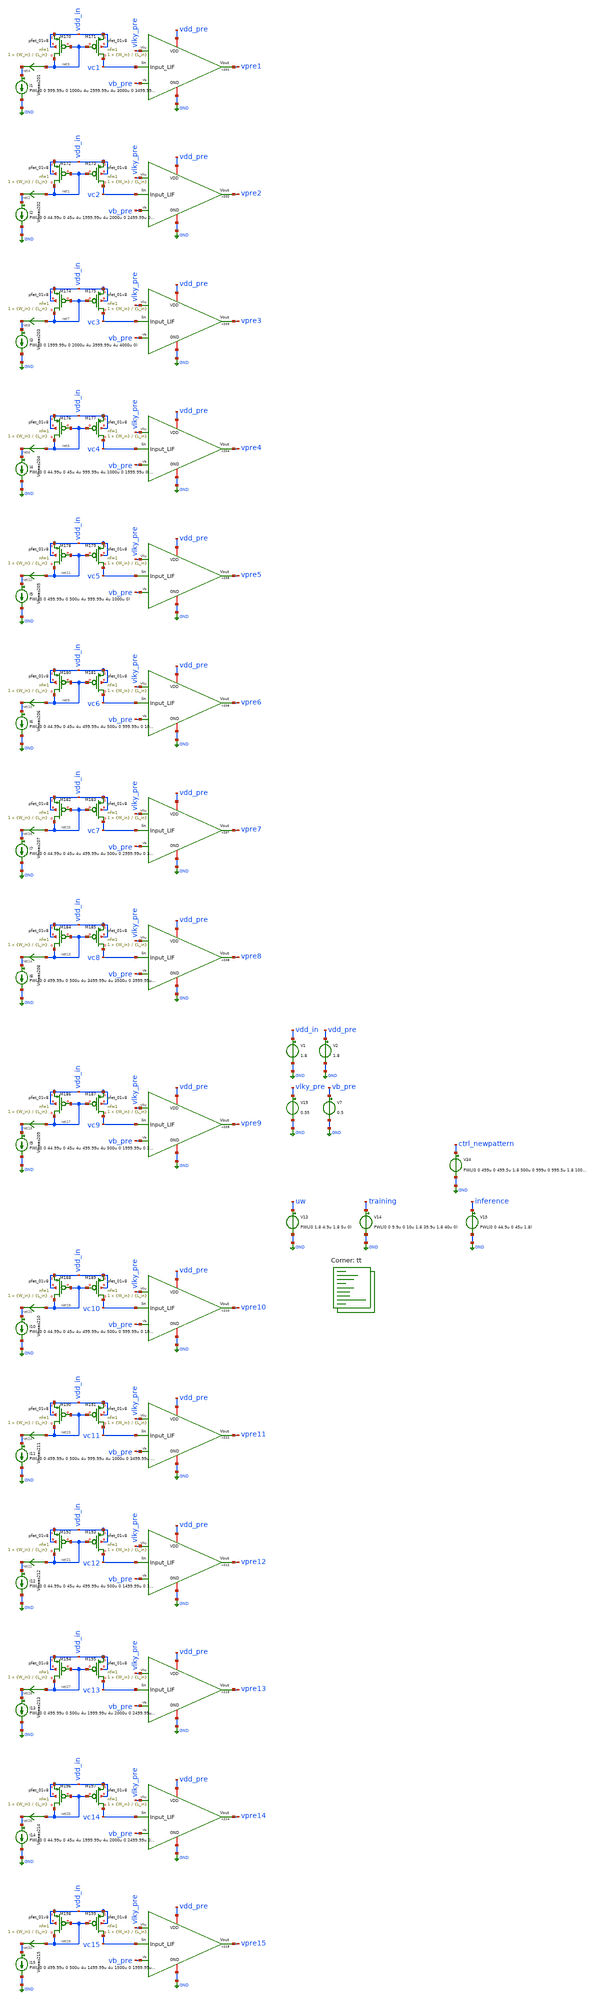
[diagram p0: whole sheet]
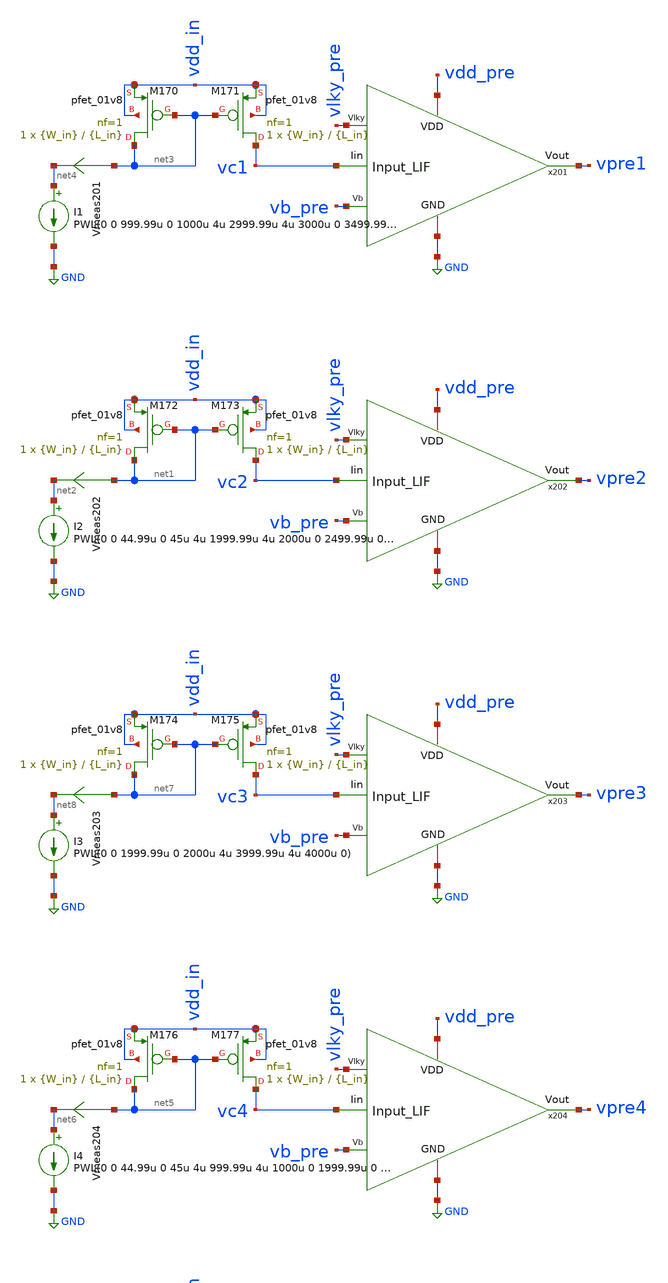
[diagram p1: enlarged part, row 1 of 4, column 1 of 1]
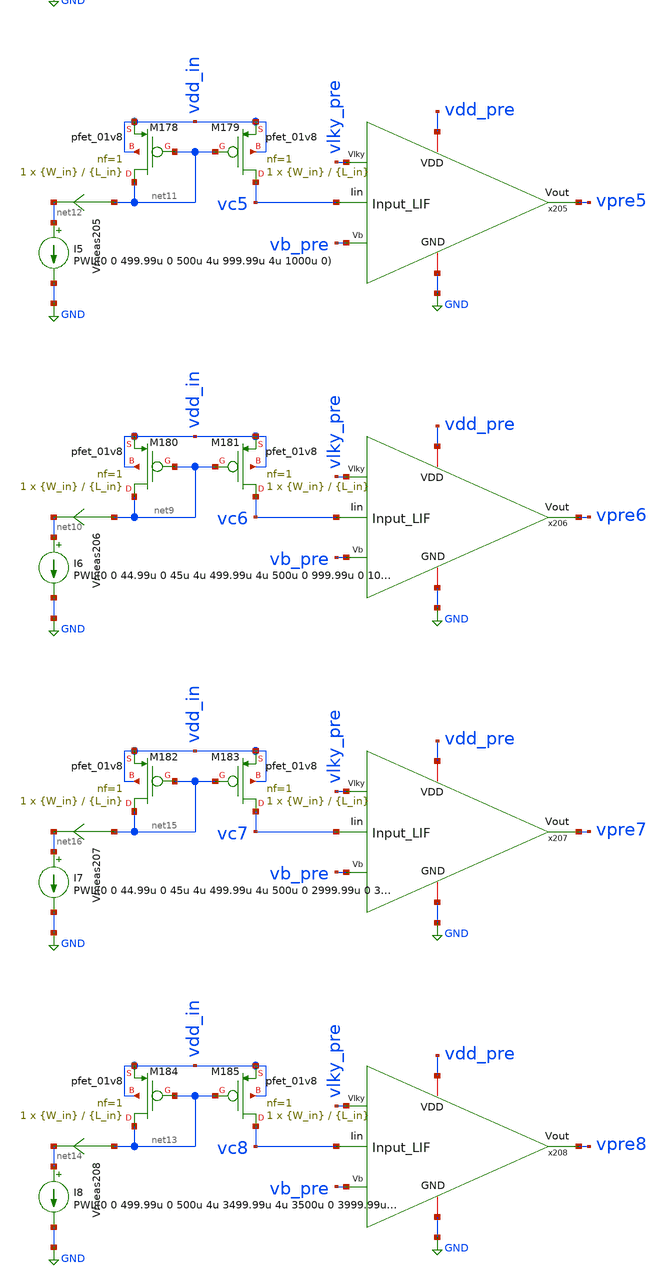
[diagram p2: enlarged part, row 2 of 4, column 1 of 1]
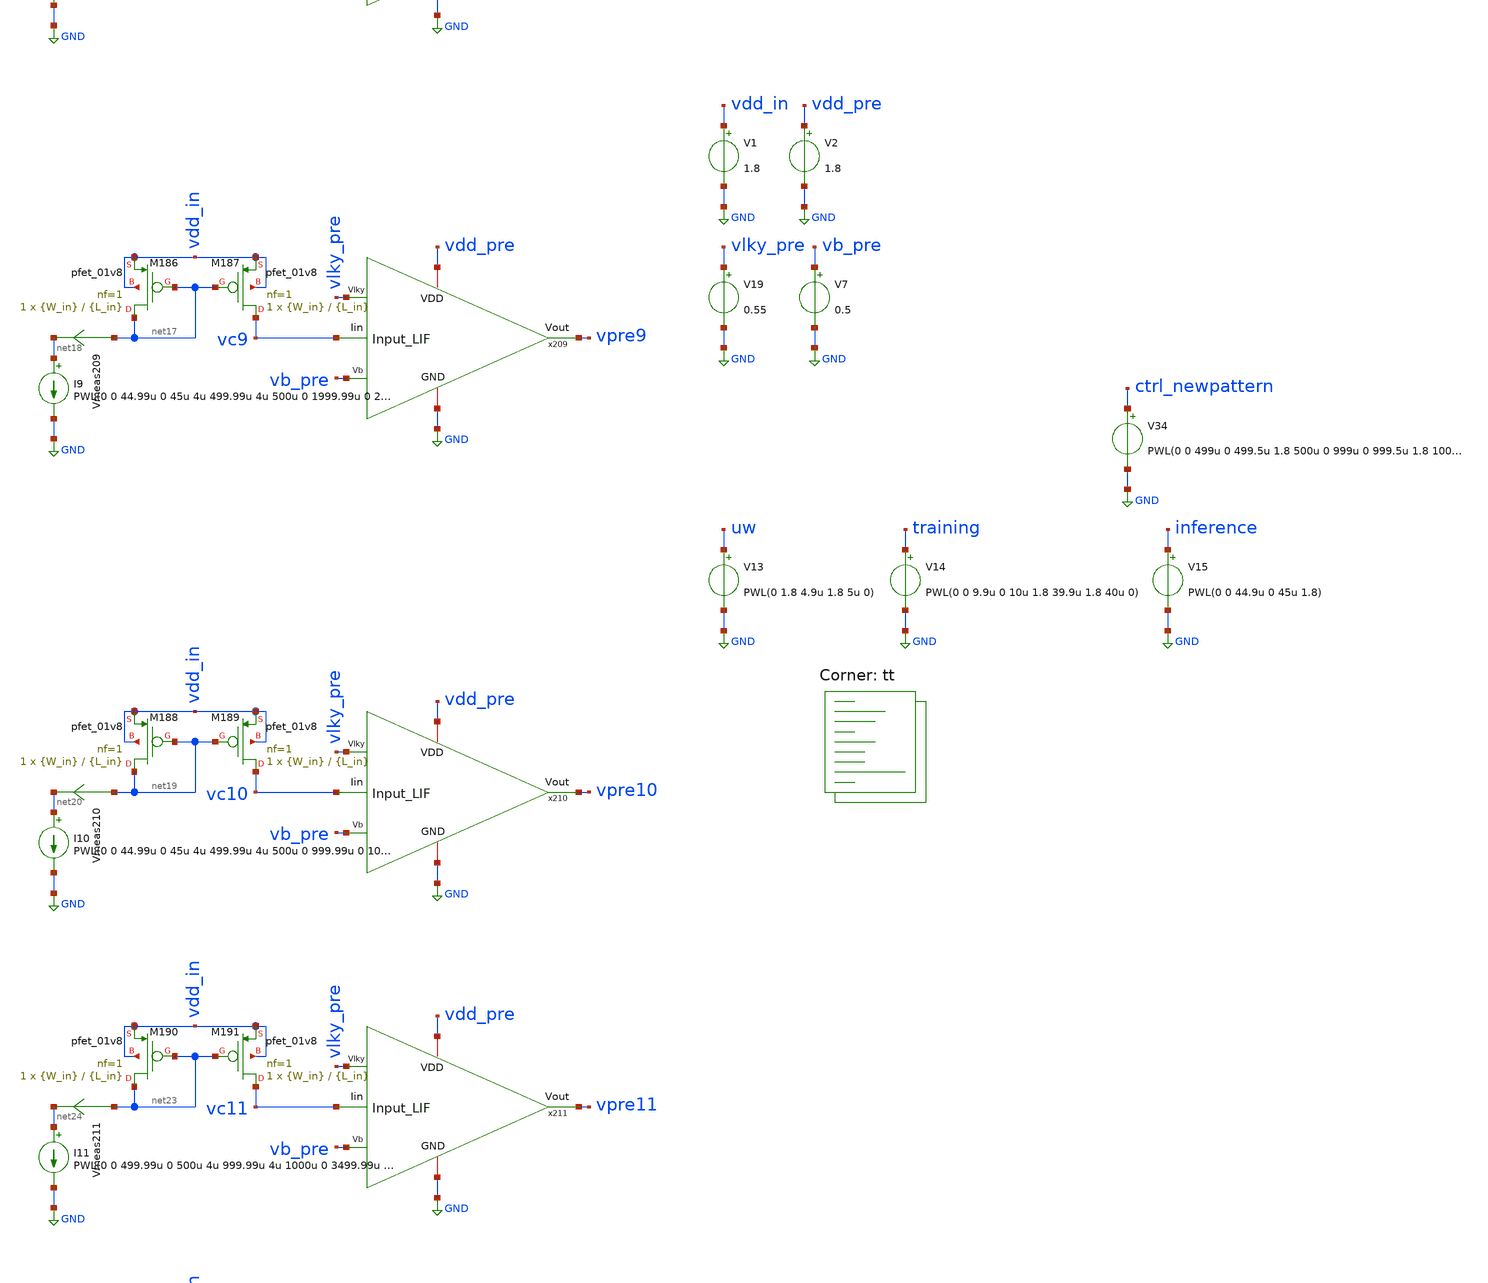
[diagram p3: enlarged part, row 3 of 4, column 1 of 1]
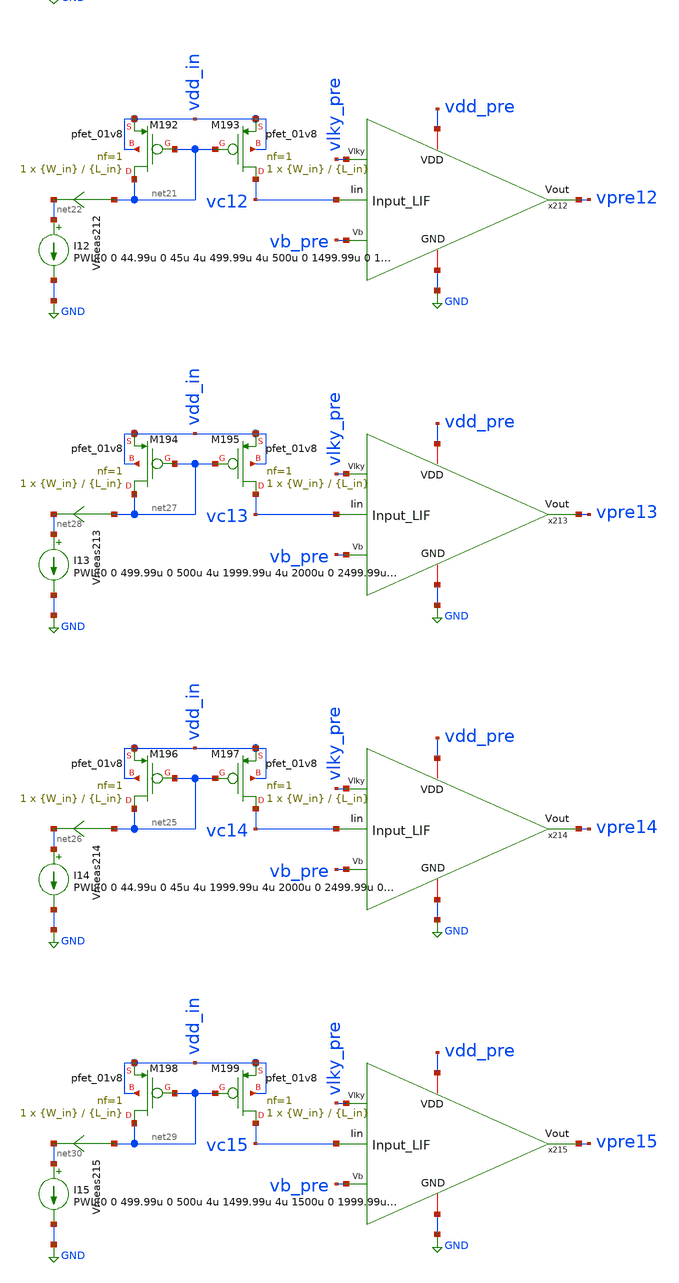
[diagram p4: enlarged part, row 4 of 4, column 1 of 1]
** sch_path: SNN/LIF_15Inputs_tb.sch
**.subckt LIF_15Inputs_tb
V1 vdd_in GND 1.8
V2 vdd_pre GND 1.8
I2 net2 GND PWL(0 0 44.99u 0 45u 4u 1999.99u 4u 2000u 0 2499.99u 0 2500u 4u)
XM173 vc2 net1 vdd_in vdd_in sky130_fd_pr__pfet_01v8 L={L_in} W={W_in} nf=1 ad='int((nf+1)/2) * W/nf * 0.29'
+ as='int((nf+2)/2) * W/nf * 0.29' pd='2*int((nf+1)/2) * (W/nf + 0.29)' ps='2*int((nf+2)/2) * (W/nf + 0.29)'
+ nrd='0.29 / W' nrs='0.29 / W' sa=0 sb=0 sd=0 mult=1 m=1
XM172 net1 net1 vdd_in vdd_in sky130_fd_pr__pfet_01v8 L={L_in} W={W_in} nf=1 ad='int((nf+1)/2) * W/nf * 0.29'
+ as='int((nf+2)/2) * W/nf * 0.29' pd='2*int((nf+1)/2) * (W/nf + 0.29)' ps='2*int((nf+2)/2) * (W/nf + 0.29)'
+ nrd='0.29 / W' nrs='0.29 / W' sa=0 sb=0 sd=0 mult=1 m=1
V13 uw GND PWL(0 1.8 4.9u 1.8 5u 0)
V14 training GND PWL(0 0 9.9u 0 10u 1.8 39.9u 1.8 40u 0)
V15 inference GND PWL(0 0 44.9u 0 45u 1.8)
Vmeas202 net1 net2 0
.save i(vmeas202)
V7 vb_pre GND 0.5
I1 net4 GND PWL(0 0 999.99u 0 1000u 4u 2999.99u 4u 3000u 0 3499.99u 0 3500u 4u 3999.99u 4u 4000u 0)
XM171 vc1 net3 vdd_in vdd_in sky130_fd_pr__pfet_01v8 L={L_in} W={W_in} nf=1 ad='int((nf+1)/2) * W/nf * 0.29'
+ as='int((nf+2)/2) * W/nf * 0.29' pd='2*int((nf+1)/2) * (W/nf + 0.29)' ps='2*int((nf+2)/2) * (W/nf + 0.29)'
+ nrd='0.29 / W' nrs='0.29 / W' sa=0 sb=0 sd=0 mult=1 m=1
XM170 net3 net3 vdd_in vdd_in sky130_fd_pr__pfet_01v8 L={L_in} W={W_in} nf=1 ad='int((nf+1)/2) * W/nf * 0.29'
+ as='int((nf+2)/2) * W/nf * 0.29' pd='2*int((nf+1)/2) * (W/nf + 0.29)' ps='2*int((nf+2)/2) * (W/nf + 0.29)'
+ nrd='0.29 / W' nrs='0.29 / W' sa=0 sb=0 sd=0 mult=1 m=1
Vmeas201 net3 net4 0
.save i(vmeas201)
V19 vlky_pre GND 0.55
I4 net6 GND PWL(0 0 44.99u 0 45u 4u 999.99u 4u 1000u 0 1999.99u 0 2000u 4u 3499.99u 4u 3500u 0
+ 3999.99u 0 4000u 4u)
XM177 vc4 net5 vdd_in vdd_in sky130_fd_pr__pfet_01v8 L={L_in} W={W_in} nf=1 ad='int((nf+1)/2) * W/nf * 0.29'
+ as='int((nf+2)/2) * W/nf * 0.29' pd='2*int((nf+1)/2) * (W/nf + 0.29)' ps='2*int((nf+2)/2) * (W/nf + 0.29)'
+ nrd='0.29 / W' nrs='0.29 / W' sa=0 sb=0 sd=0 mult=1 m=1
XM176 net5 net5 vdd_in vdd_in sky130_fd_pr__pfet_01v8 L={L_in} W={W_in} nf=1 ad='int((nf+1)/2) * W/nf * 0.29'
+ as='int((nf+2)/2) * W/nf * 0.29' pd='2*int((nf+1)/2) * (W/nf + 0.29)' ps='2*int((nf+2)/2) * (W/nf + 0.29)'
+ nrd='0.29 / W' nrs='0.29 / W' sa=0 sb=0 sd=0 mult=1 m=1
Vmeas204 net5 net6 0
.save i(vmeas204)
I3 net8 GND PWL(0 0 1999.99u 0 2000u 4u 3999.99u 4u 4000u 0)
XM175 vc3 net7 vdd_in vdd_in sky130_fd_pr__pfet_01v8 L={L_in} W={W_in} nf=1 ad='int((nf+1)/2) * W/nf * 0.29'
+ as='int((nf+2)/2) * W/nf * 0.29' pd='2*int((nf+1)/2) * (W/nf + 0.29)' ps='2*int((nf+2)/2) * (W/nf + 0.29)'
+ nrd='0.29 / W' nrs='0.29 / W' sa=0 sb=0 sd=0 mult=1 m=1
XM174 net7 net7 vdd_in vdd_in sky130_fd_pr__pfet_01v8 L={L_in} W={W_in} nf=1 ad='int((nf+1)/2) * W/nf * 0.29'
+ as='int((nf+2)/2) * W/nf * 0.29' pd='2*int((nf+1)/2) * (W/nf + 0.29)' ps='2*int((nf+2)/2) * (W/nf + 0.29)'
+ nrd='0.29 / W' nrs='0.29 / W' sa=0 sb=0 sd=0 mult=1 m=1
Vmeas203 net7 net8 0
.save i(vmeas203)
I6 net10 GND PWL(0 0 44.99u 0 45u 4u 499.99u 4u 500u 0 999.99u 0 1000u 4u 2499.99u 4u 2500u 0
+ 3499.99u 0 3500u 4u)
XM181 vc6 net9 vdd_in vdd_in sky130_fd_pr__pfet_01v8 L={L_in} W={W_in} nf=1 ad='int((nf+1)/2) * W/nf * 0.29'
+ as='int((nf+2)/2) * W/nf * 0.29' pd='2*int((nf+1)/2) * (W/nf + 0.29)' ps='2*int((nf+2)/2) * (W/nf + 0.29)'
+ nrd='0.29 / W' nrs='0.29 / W' sa=0 sb=0 sd=0 mult=1 m=1
XM180 net9 net9 vdd_in vdd_in sky130_fd_pr__pfet_01v8 L={L_in} W={W_in} nf=1 ad='int((nf+1)/2) * W/nf * 0.29'
+ as='int((nf+2)/2) * W/nf * 0.29' pd='2*int((nf+1)/2) * (W/nf + 0.29)' ps='2*int((nf+2)/2) * (W/nf + 0.29)'
+ nrd='0.29 / W' nrs='0.29 / W' sa=0 sb=0 sd=0 mult=1 m=1
Vmeas206 net9 net10 0
.save i(vmeas206)
I5 net12 GND PWL(0 0 499.99u 0 500u 4u 999.99u 4u 1000u 0)
XM179 vc5 net11 vdd_in vdd_in sky130_fd_pr__pfet_01v8 L={L_in} W={W_in} nf=1 ad='int((nf+1)/2) * W/nf * 0.29'
+ as='int((nf+2)/2) * W/nf * 0.29' pd='2*int((nf+1)/2) * (W/nf + 0.29)' ps='2*int((nf+2)/2) * (W/nf + 0.29)'
+ nrd='0.29 / W' nrs='0.29 / W' sa=0 sb=0 sd=0 mult=1 m=1
XM178 net11 net11 vdd_in vdd_in sky130_fd_pr__pfet_01v8 L={L_in} W={W_in} nf=1 ad='int((nf+1)/2) * W/nf * 0.29'
+ as='int((nf+2)/2) * W/nf * 0.29' pd='2*int((nf+1)/2) * (W/nf + 0.29)' ps='2*int((nf+2)/2) * (W/nf + 0.29)'
+ nrd='0.29 / W' nrs='0.29 / W' sa=0 sb=0 sd=0 mult=1 m=1
Vmeas205 net11 net12 0
.save i(vmeas205)
I8 net14 GND PWL(0 0 499.99u 0 500u 4u 3499.99u 4u 3500u 0 3999.99u 0 4000u 4u)
XM185 vc8 net13 vdd_in vdd_in sky130_fd_pr__pfet_01v8 L={L_in} W={W_in} nf=1 ad='int((nf+1)/2) * W/nf * 0.29'
+ as='int((nf+2)/2) * W/nf * 0.29' pd='2*int((nf+1)/2) * (W/nf + 0.29)' ps='2*int((nf+2)/2) * (W/nf + 0.29)'
+ nrd='0.29 / W' nrs='0.29 / W' sa=0 sb=0 sd=0 mult=1 m=1
XM184 net13 net13 vdd_in vdd_in sky130_fd_pr__pfet_01v8 L={L_in} W={W_in} nf=1 ad='int((nf+1)/2) * W/nf * 0.29'
+ as='int((nf+2)/2) * W/nf * 0.29' pd='2*int((nf+1)/2) * (W/nf + 0.29)' ps='2*int((nf+2)/2) * (W/nf + 0.29)'
+ nrd='0.29 / W' nrs='0.29 / W' sa=0 sb=0 sd=0 mult=1 m=1
Vmeas208 net13 net14 0
.save i(vmeas208)
I7 net16 GND PWL(0 0 44.99u 0 45u 4u 499.99u 4u 500u 0 2999.99u 0 3000u 4u 3499.99u 4u 3500u 0)
XM183 vc7 net15 vdd_in vdd_in sky130_fd_pr__pfet_01v8 L={L_in} W={W_in} nf=1 ad='int((nf+1)/2) * W/nf * 0.29'
+ as='int((nf+2)/2) * W/nf * 0.29' pd='2*int((nf+1)/2) * (W/nf + 0.29)' ps='2*int((nf+2)/2) * (W/nf + 0.29)'
+ nrd='0.29 / W' nrs='0.29 / W' sa=0 sb=0 sd=0 mult=1 m=1
XM182 net15 net15 vdd_in vdd_in sky130_fd_pr__pfet_01v8 L={L_in} W={W_in} nf=1 ad='int((nf+1)/2) * W/nf * 0.29'
+ as='int((nf+2)/2) * W/nf * 0.29' pd='2*int((nf+1)/2) * (W/nf + 0.29)' ps='2*int((nf+2)/2) * (W/nf + 0.29)'
+ nrd='0.29 / W' nrs='0.29 / W' sa=0 sb=0 sd=0 mult=1 m=1
Vmeas207 net15 net16 0
.save i(vmeas207)
I9 net18 GND PWL(0 0 44.99u 0 45u 4u 499.99u 4u 500u 0 1999.99u 0 2000u 4u 2499.99u 4u 2500u 0
+ 3499.99u 0 3500u 4u 3999.99u 4u 4000u 0 4499.99u 0 4500u 4u)
XM187 vc9 net17 vdd_in vdd_in sky130_fd_pr__pfet_01v8 L={L_in} W={W_in} nf=1 ad='int((nf+1)/2) * W/nf * 0.29'
+ as='int((nf+2)/2) * W/nf * 0.29' pd='2*int((nf+1)/2) * (W/nf + 0.29)' ps='2*int((nf+2)/2) * (W/nf + 0.29)'
+ nrd='0.29 / W' nrs='0.29 / W' sa=0 sb=0 sd=0 mult=1 m=1
XM186 net17 net17 vdd_in vdd_in sky130_fd_pr__pfet_01v8 L={L_in} W={W_in} nf=1 ad='int((nf+1)/2) * W/nf * 0.29'
+ as='int((nf+2)/2) * W/nf * 0.29' pd='2*int((nf+1)/2) * (W/nf + 0.29)' ps='2*int((nf+2)/2) * (W/nf + 0.29)'
+ nrd='0.29 / W' nrs='0.29 / W' sa=0 sb=0 sd=0 mult=1 m=1
Vmeas209 net17 net18 0
.save i(vmeas209)
I10 net20 GND PWL(0 0 44.99u 0 45u 4u 499.99u 4u 500u 0 999.99u 0 1000u 4u 1499.99u 4u 1500u 0
+ 2999.99u 0 3000u 4u 3499.99u 4u 3500u 0 3999.99u 0 4000u 4u 4499.99u 4u 4500u 0)
XM189 vc10 net19 vdd_in vdd_in sky130_fd_pr__pfet_01v8 L={L_in} W={W_in} nf=1 ad='int((nf+1)/2) * W/nf * 0.29'
+ as='int((nf+2)/2) * W/nf * 0.29' pd='2*int((nf+1)/2) * (W/nf + 0.29)' ps='2*int((nf+2)/2) * (W/nf + 0.29)'
+ nrd='0.29 / W' nrs='0.29 / W' sa=0 sb=0 sd=0 mult=1 m=1
XM188 net19 net19 vdd_in vdd_in sky130_fd_pr__pfet_01v8 L={L_in} W={W_in} nf=1 ad='int((nf+1)/2) * W/nf * 0.29'
+ as='int((nf+2)/2) * W/nf * 0.29' pd='2*int((nf+1)/2) * (W/nf + 0.29)' ps='2*int((nf+2)/2) * (W/nf + 0.29)'
+ nrd='0.29 / W' nrs='0.29 / W' sa=0 sb=0 sd=0 mult=1 m=1
Vmeas210 net19 net20 0
.save i(vmeas210)
I12 net22 GND PWL(0 0 44.99u 0 45u 4u 499.99u 4u 500u 0 1499.99u 0 1500u 4u 3499.99u 4u 3500u 0
+ 3999.99u 0 4000u 4u)
XM193 vc12 net21 vdd_in vdd_in sky130_fd_pr__pfet_01v8 L={L_in} W={W_in} nf=1 ad='int((nf+1)/2) * W/nf * 0.29'
+ as='int((nf+2)/2) * W/nf * 0.29' pd='2*int((nf+1)/2) * (W/nf + 0.29)' ps='2*int((nf+2)/2) * (W/nf + 0.29)'
+ nrd='0.29 / W' nrs='0.29 / W' sa=0 sb=0 sd=0 mult=1 m=1
XM192 net21 net21 vdd_in vdd_in sky130_fd_pr__pfet_01v8 L={L_in} W={W_in} nf=1 ad='int((nf+1)/2) * W/nf * 0.29'
+ as='int((nf+2)/2) * W/nf * 0.29' pd='2*int((nf+1)/2) * (W/nf + 0.29)' ps='2*int((nf+2)/2) * (W/nf + 0.29)'
+ nrd='0.29 / W' nrs='0.29 / W' sa=0 sb=0 sd=0 mult=1 m=1
Vmeas212 net21 net22 0
.save i(vmeas212)
I11 net24 GND PWL(0 0 499.99u 0 500u 4u 999.99u 4u 1000u 0 3499.99u 0 3500u 4u 3999.99u 4u 4000u 0)
XM191 vc11 net23 vdd_in vdd_in sky130_fd_pr__pfet_01v8 L={L_in} W={W_in} nf=1 ad='int((nf+1)/2) * W/nf * 0.29'
+ as='int((nf+2)/2) * W/nf * 0.29' pd='2*int((nf+1)/2) * (W/nf + 0.29)' ps='2*int((nf+2)/2) * (W/nf + 0.29)'
+ nrd='0.29 / W' nrs='0.29 / W' sa=0 sb=0 sd=0 mult=1 m=1
XM190 net23 net23 vdd_in vdd_in sky130_fd_pr__pfet_01v8 L={L_in} W={W_in} nf=1 ad='int((nf+1)/2) * W/nf * 0.29'
+ as='int((nf+2)/2) * W/nf * 0.29' pd='2*int((nf+1)/2) * (W/nf + 0.29)' ps='2*int((nf+2)/2) * (W/nf + 0.29)'
+ nrd='0.29 / W' nrs='0.29 / W' sa=0 sb=0 sd=0 mult=1 m=1
Vmeas211 net23 net24 0
.save i(vmeas211)
I14 net26 GND PWL(0 0 44.99u 0 45u 4u 1999.99u 4u 2000u 0 2499.99u 0 2500u 4u 3499.99u 4u 3500u 0
+ 3999.99u 0 4000u 4u 4499.99u 4u 4500u 0)
XM197 vc14 net25 vdd_in vdd_in sky130_fd_pr__pfet_01v8 L={L_in} W={W_in} nf=1 ad='int((nf+1)/2) * W/nf * 0.29'
+ as='int((nf+2)/2) * W/nf * 0.29' pd='2*int((nf+1)/2) * (W/nf + 0.29)' ps='2*int((nf+2)/2) * (W/nf + 0.29)'
+ nrd='0.29 / W' nrs='0.29 / W' sa=0 sb=0 sd=0 mult=1 m=1
XM196 net25 net25 vdd_in vdd_in sky130_fd_pr__pfet_01v8 L={L_in} W={W_in} nf=1 ad='int((nf+1)/2) * W/nf * 0.29'
+ as='int((nf+2)/2) * W/nf * 0.29' pd='2*int((nf+1)/2) * (W/nf + 0.29)' ps='2*int((nf+2)/2) * (W/nf + 0.29)'
+ nrd='0.29 / W' nrs='0.29 / W' sa=0 sb=0 sd=0 mult=1 m=1
Vmeas214 net25 net26 0
.save i(vmeas214)
I13 net28 GND PWL(0 0 499.99u 0 500u 4u 1999.99u 4u 2000u 0 2499.99u 0 2500u 4u 2999.99u 4u 3000u 0
+ 3499.99u 0 3500u 4u 3999.99u 4u 4000u 0)
XM195 vc13 net27 vdd_in vdd_in sky130_fd_pr__pfet_01v8 L={L_in} W={W_in} nf=1 ad='int((nf+1)/2) * W/nf * 0.29'
+ as='int((nf+2)/2) * W/nf * 0.29' pd='2*int((nf+1)/2) * (W/nf + 0.29)' ps='2*int((nf+2)/2) * (W/nf + 0.29)'
+ nrd='0.29 / W' nrs='0.29 / W' sa=0 sb=0 sd=0 mult=1 m=1
XM194 net27 net27 vdd_in vdd_in sky130_fd_pr__pfet_01v8 L={L_in} W={W_in} nf=1 ad='int((nf+1)/2) * W/nf * 0.29'
+ as='int((nf+2)/2) * W/nf * 0.29' pd='2*int((nf+1)/2) * (W/nf + 0.29)' ps='2*int((nf+2)/2) * (W/nf + 0.29)'
+ nrd='0.29 / W' nrs='0.29 / W' sa=0 sb=0 sd=0 mult=1 m=1
Vmeas213 net27 net28 0
.save i(vmeas213)
I15 net30 GND PWL(0 0 499.99u 0 500u 4u 1499.99u 4u 1500u 0 1999.99u 0 2000u 4u 2499.99u 4u 2500u 0
+ 4499.99u 0 4500u 4u)
XM199 vc15 net29 vdd_in vdd_in sky130_fd_pr__pfet_01v8 L={L_in} W={W_in} nf=1 ad='int((nf+1)/2) * W/nf * 0.29'
+ as='int((nf+2)/2) * W/nf * 0.29' pd='2*int((nf+1)/2) * (W/nf + 0.29)' ps='2*int((nf+2)/2) * (W/nf + 0.29)'
+ nrd='0.29 / W' nrs='0.29 / W' sa=0 sb=0 sd=0 mult=1 m=1
XM198 net29 net29 vdd_in vdd_in sky130_fd_pr__pfet_01v8 L={L_in} W={W_in} nf=1 ad='int((nf+1)/2) * W/nf * 0.29'
+ as='int((nf+2)/2) * W/nf * 0.29' pd='2*int((nf+1)/2) * (W/nf + 0.29)' ps='2*int((nf+2)/2) * (W/nf + 0.29)'
+ nrd='0.29 / W' nrs='0.29 / W' sa=0 sb=0 sd=0 mult=1 m=1
Vmeas215 net29 net30 0
.save i(vmeas215)
V34 ctrl_newpattern GND PWL(0 0 499u 0 499.5u 1.8 500u 0 999u 0 999.5u 1.8 1000u 0 1499u 0 1499.5u
+ 1.8 1500u 0 1999u 0 1999.5u 1.8 2000u 0 2499u 0 2499.5u 1.8 2500u 0 2999u 0 2999.5u 1.8 3000u 0 3499u 0
+ 3499.5u 1.8 3500u 0 3999u 0 3999.5u 1.8 4000u 0 4499u 0 4499.5u 1.8 4500u 0)
x201 vlky_pre vb_pre vdd_pre vpre1 GND vc1 Input_LIF
x202 vlky_pre vb_pre vdd_pre vpre2 GND vc2 Input_LIF
x203 vlky_pre vb_pre vdd_pre vpre3 GND vc3 Input_LIF
x204 vlky_pre vb_pre vdd_pre vpre4 GND vc4 Input_LIF
x205 vlky_pre vb_pre vdd_pre vpre5 GND vc5 Input_LIF
x206 vlky_pre vb_pre vdd_pre vpre6 GND vc6 Input_LIF
x207 vlky_pre vb_pre vdd_pre vpre7 GND vc7 Input_LIF
x208 vlky_pre vb_pre vdd_pre vpre8 GND vc8 Input_LIF
x209 vlky_pre vb_pre vdd_pre vpre9 GND vc9 Input_LIF
x210 vlky_pre vb_pre vdd_pre vpre10 GND vc10 Input_LIF
x211 vlky_pre vb_pre vdd_pre vpre11 GND vc11 Input_LIF
x212 vlky_pre vb_pre vdd_pre vpre12 GND vc12 Input_LIF
x213 vlky_pre vb_pre vdd_pre vpre13 GND vc13 Input_LIF
x214 vlky_pre vb_pre vdd_pre vpre14 GND vc14 Input_LIF
x215 vlky_pre vb_pre vdd_pre vpre15 GND vc15 Input_LIF
**** begin user architecture code
.lib $::SKYWATER_MODELS/sky130.lib.spice tt

** opencircuitdesign pdks install
.inc $::SKYWATER_MODELS/rram_v0.spice



.option set_threads = 16
.option klu
*--Current Injection--*
.param L_in=0.15
.param W_in=1
.control
	save all
	tran 100n 5000u 0
	write LIF_15Inputs_tb2.raw v(vpre1) v(vpre2) v(vpre3) v(vpre4) v(vpre5) v(vpre6) v(vpre7) v(vpre8)
+ v(vpre9) v(vpre10) v(vpre11) v(vpre12) v(vpre13) v(vpre14) v(vpre15) v(ctrl_newpattern)
	*wrdata SNN_15x1_lt_tb.ssv v(8)
.endc


**** end user architecture code
**.ends

* expanding   symbol:  /home/ricardo/RATT_repos/Proyectos_xschem/SNN/Input_LIF.sym # of pins=6
** sym_path: Final_Design/Input_LIF.sym
** sch_path: Final_Design/Input_LIF.sch
.subckt Input_LIF Vlky Vb VDD Vout GND Iin
*.iopin GND
*.ipin Vb
*.iopin VDD
*.opin Vout
*.ipin Iin
*.ipin Vlky
XM5 net3 Vb GND GND sky130_fd_pr__nfet_01v8 L=0.15 W=5 nf=1 ad='int((nf+1)/2) * W/nf * 0.29' as='int((nf+2)/2) * W/nf * 0.29'
+ pd='2*int((nf+1)/2) * (W/nf + 0.29)' ps='2*int((nf+2)/2) * (W/nf + 0.29)' nrd='0.29 / W' nrs='0.29 / W'
+ sa=0 sb=0 sd=0 mult=1 m=1
XM4 net1 net2 net3 GND sky130_fd_pr__nfet_01v8 L=0.15 W=1.5 nf=1 ad='int((nf+1)/2) * W/nf * 0.29' as='int((nf+2)/2) * W/nf * 0.29'
+ pd='2*int((nf+1)/2) * (W/nf + 0.29)' ps='2*int((nf+2)/2) * (W/nf + 0.29)' nrd='0.29 / W' nrs='0.29 / W'
+ sa=0 sb=0 sd=0 mult=1 m=1
XM3 net1 net2 VDD VDD sky130_fd_pr__pfet_01v8 L=20 W=1 nf=1 ad='int((nf+1)/2) * W/nf * 0.29' as='int((nf+2)/2) * W/nf * 0.29'
+ pd='2*int((nf+1)/2) * (W/nf + 0.29)' ps='2*int((nf+2)/2) * (W/nf + 0.29)' nrd='0.29 / W' nrs='0.29 / W'
+ sa=0 sb=0 sd=0 mult=1 m=1
XC2 net1 GND sky130_fd_pr__cap_mim_m3_1 W=10 L=5 MF=1 m=1
XM2 Iin net1 GND GND sky130_fd_pr__nfet_01v8 L=20 W=1 nf=1 ad='int((nf+1)/2) * W/nf * 0.29' as='int((nf+2)/2) * W/nf * 0.29'
+ pd='2*int((nf+1)/2) * (W/nf + 0.29)' ps='2*int((nf+2)/2) * (W/nf + 0.29)' nrd='0.29 / W' nrs='0.29 / W'
+ sa=0 sb=0 sd=0 mult=1 m=1
XC1 Iin GND sky130_fd_pr__cap_mim_m3_1 W=20 L=20 MF=1 m=1
XM10 net4 Vout GND GND sky130_fd_pr__nfet_01v8 L=0.15 W=1.5 nf=1 ad='int((nf+1)/2) * W/nf * 0.29' as='int((nf+2)/2) * W/nf * 0.29'
+ pd='2*int((nf+1)/2) * (W/nf + 0.29)' ps='2*int((nf+2)/2) * (W/nf + 0.29)' nrd='0.29 / W' nrs='0.29 / W'
+ sa=0 sb=0 sd=0 mult=1 m=1
XM7 net2 Iin net4 GND sky130_fd_pr__nfet_01v8 L=0.15 W=1.5 nf=1 ad='int((nf+1)/2) * W/nf * 0.29' as='int((nf+2)/2) * W/nf * 0.29'
+ pd='2*int((nf+1)/2) * (W/nf + 0.29)' ps='2*int((nf+2)/2) * (W/nf + 0.29)' nrd='0.29 / W' nrs='0.29 / W'
+ sa=0 sb=0 sd=0 mult=1 m=1
XM6 net2 Iin VDD VDD sky130_fd_pr__pfet_01v8 L=0.15 W=1.5 nf=1 ad='int((nf+1)/2) * W/nf * 0.29' as='int((nf+2)/2) * W/nf * 0.29'
+ pd='2*int((nf+1)/2) * (W/nf + 0.29)' ps='2*int((nf+2)/2) * (W/nf + 0.29)' nrd='0.29 / W' nrs='0.29 / W'
+ sa=0 sb=0 sd=0 mult=1 m=1
XM9 Vout net2 net4 GND sky130_fd_pr__nfet_01v8 L=0.15 W=1.5 nf=1 ad='int((nf+1)/2) * W/nf * 0.29' as='int((nf+2)/2) * W/nf * 0.29'
+ pd='2*int((nf+1)/2) * (W/nf + 0.29)' ps='2*int((nf+2)/2) * (W/nf + 0.29)' nrd='0.29 / W' nrs='0.29 / W'
+ sa=0 sb=0 sd=0 mult=1 m=1
XM8 Vout net2 VDD VDD sky130_fd_pr__pfet_01v8 L=0.15 W=5 nf=1 ad='int((nf+1)/2) * W/nf * 0.29' as='int((nf+2)/2) * W/nf * 0.29'
+ pd='2*int((nf+1)/2) * (W/nf + 0.29)' ps='2*int((nf+2)/2) * (W/nf + 0.29)' nrd='0.29 / W' nrs='0.29 / W'
+ sa=0 sb=0 sd=0 mult=1 m=1
XM1 Iin Vlky GND GND sky130_fd_pr__nfet_01v8 L=0.15 W=1.5 nf=1 ad='int((nf+1)/2) * W/nf * 0.29' as='int((nf+2)/2) * W/nf * 0.29'
+ pd='2*int((nf+1)/2) * (W/nf + 0.29)' ps='2*int((nf+2)/2) * (W/nf + 0.29)' nrd='0.29 / W' nrs='0.29 / W'
+ sa=0 sb=0 sd=0 mult=1 m=1
.ends

.GLOBAL GND
.end
